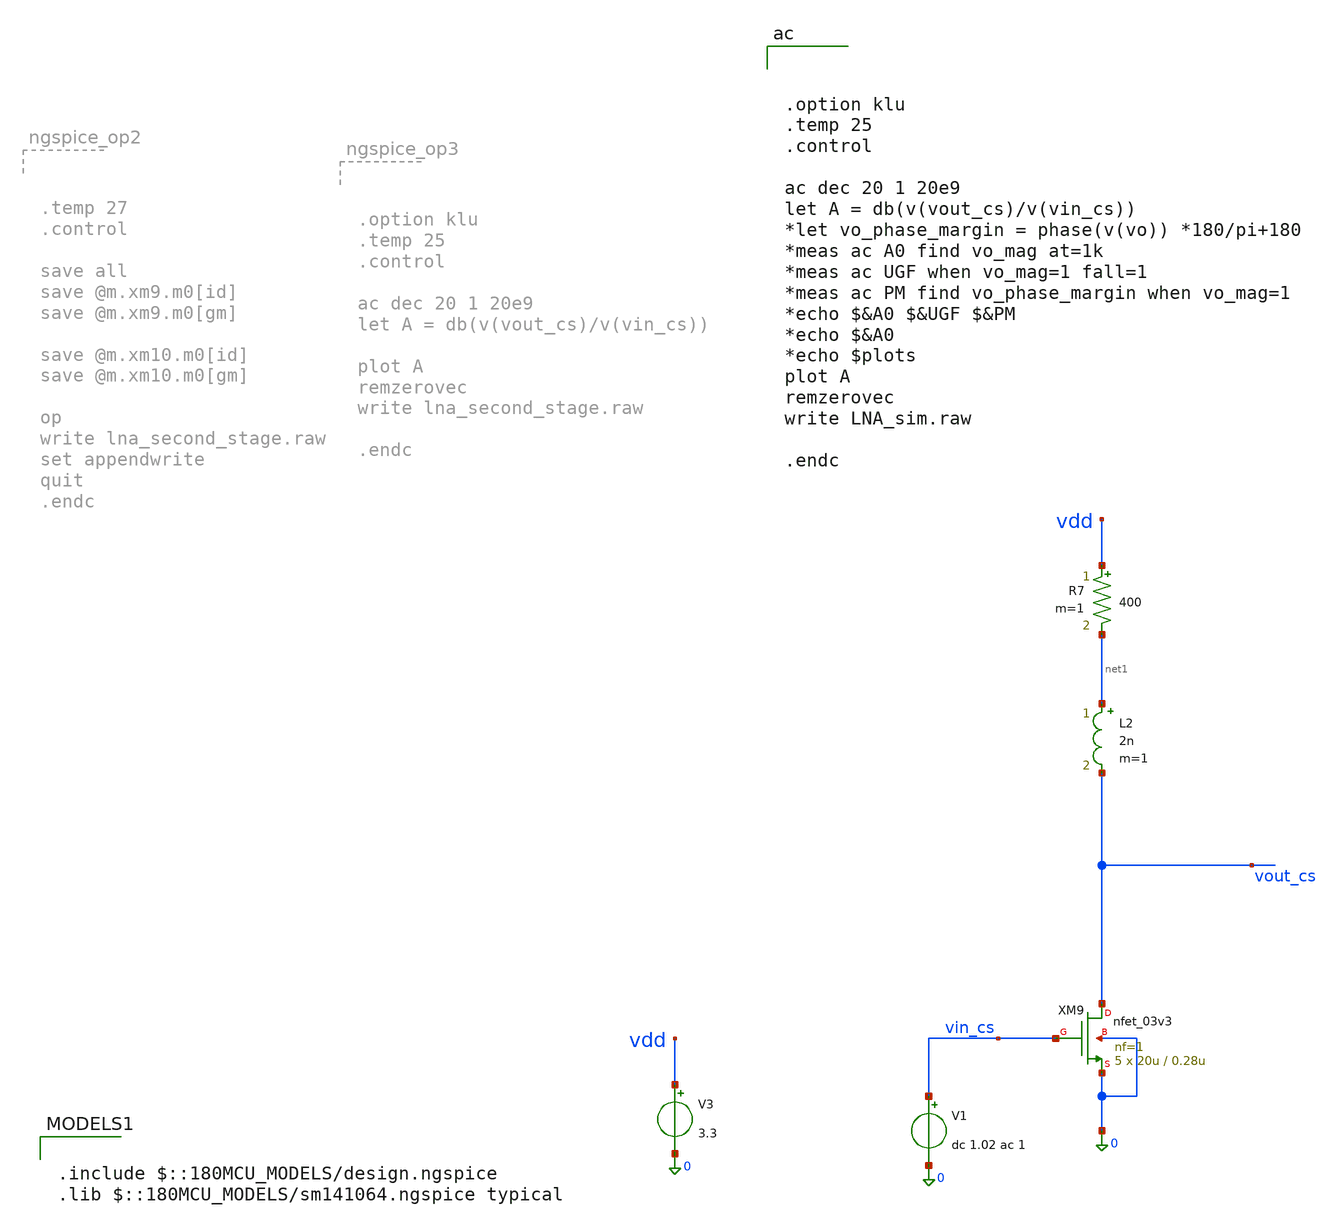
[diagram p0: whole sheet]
** sch_path: xschem/lna_second_stage.sch
**.subckt lna_second_stage
XM9 vout_cs vin_cs 0 0 nfet_03v3 L=0.28u W=20u nf=1 ad='int((nf+1)/2) * W/nf * 0.18u' as='int((nf+2)/2) * W/nf * 0.18u'
+ pd='2*int((nf+1)/2) * (W/nf + 0.18u)' ps='2*int((nf+2)/2) * (W/nf + 0.18u)' nrd='0.18u / W' nrs='0.18u / W'
+ sa=0 sb=0 sd=0 m=5
R7 vdd net1 400 m=1
V3 vdd 0 3.3
V1 vin_cs 0 dc 1.02 ac 1
L2 net1 vout_cs 2n m=1
**** begin user architecture code

.include $::180MCU_MODELS/design.ngspice
.lib $::180MCU_MODELS/sm141064.ngspice typical




.option klu
.temp 25
.control

ac dec 20 1 20e9
let A = db(v(vout_cs)/v(vin_cs))
*let vo_phase_margin = phase(v(vo)) *180/pi+180
*meas ac A0 find vo_mag at=1k
*meas ac UGF when vo_mag=1 fall=1
*meas ac PM find vo_phase_margin when vo_mag=1
*echo $&A0 $&UGF $&PM
*echo $&A0
*echo $plots
plot A
remzerovec
write LNA_sim.raw

.endc


**** end user architecture code
**.ends
.end
